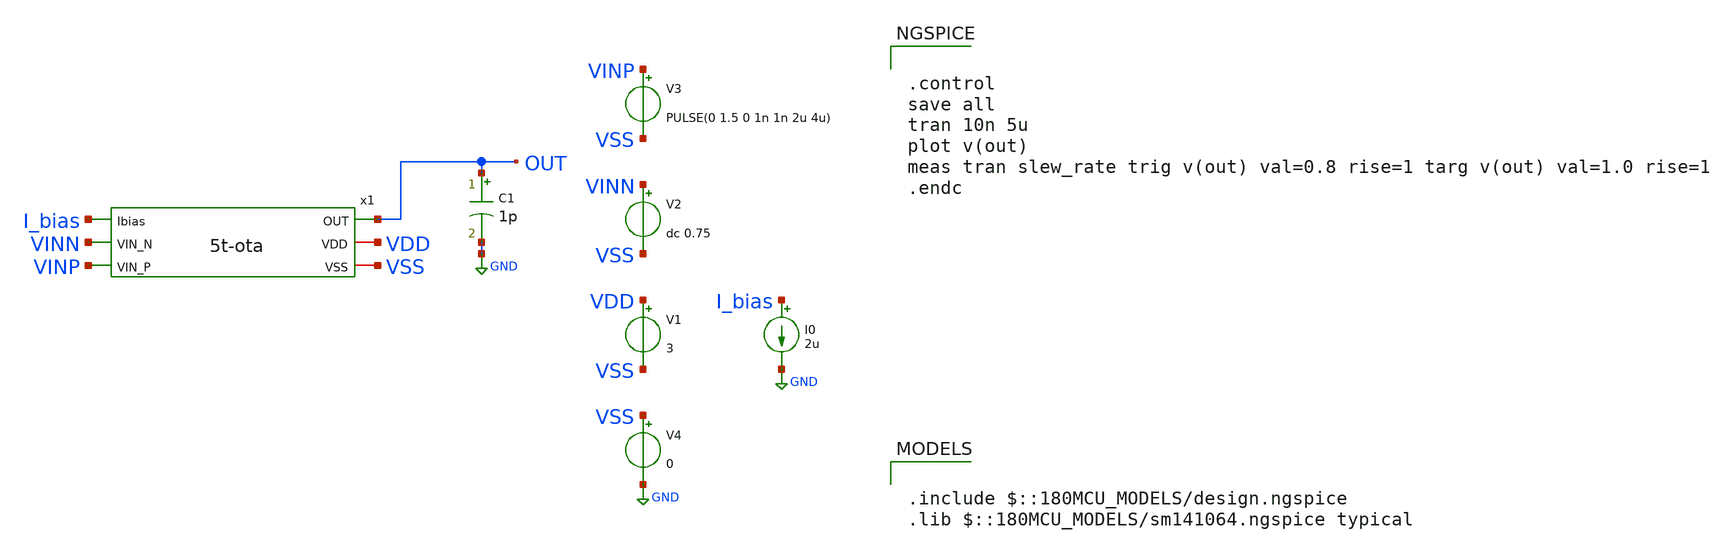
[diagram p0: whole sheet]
** sch_path: week02_current_diffpair/tugas5_cascode_current_mirror/5t-ota-psrr.sch
**.subckt 5t-ota-psrr
V1 VDD VSS 3
V2 VINN VSS dc 0.75
V3 VINP VSS PULSE(0 1.5 0 1n 1n 2u 4u)
V4 VSS GND 0
I0 I_bias GND 2u
x1 I_bias VINN VINP OUT VDD VSS 5t-ota
C1 OUT GND 1p m=1
**** begin user architecture code

.include $::180MCU_MODELS/design.ngspice
.lib $::180MCU_MODELS/sm141064.ngspice typical



.control
save all
tran 10n 5u
plot v(out)
meas tran slew_rate trig v(out) val=0.8 rise=1 targ v(out) val=1.0 rise=1
.endc


**** end user architecture code
**.ends

* expanding   symbol:  5t-ota.sym # of pins=6
** sym_path: week02_current_diffpair/tugas5_cascode_current_mirror/5t-ota.sym
** sch_path: week02_current_diffpair/tugas5_cascode_current_mirror/5t-ota.sch
.subckt 5t-ota Ibias VIN_N VIN_P OUT VDD VSS
*.ipin VIN_N
*.ipin VIN_P
*.opin OUT
*.iopin VDD
*.iopin VSS
*.ipin Ibias
XM4 net1 Ibias VSS VSS nfet_06v0 L=1u W=2.5u nf=1 ad='int((nf+1)/2) * W/nf * 0.18u' as='int((nf+2)/2) * W/nf * 0.18u'
+ pd='2*int((nf+1)/2) * (W/nf + 0.18u)' ps='2*int((nf+2)/2) * (W/nf + 0.18u)' nrd='0.18u / W' nrs='0.18u / W'
+ sa=0 sb=0 sd=0 m=1
XM8 Ibias Ibias VSS VSS nfet_06v0 L=1u W=5u nf=1 ad='int((nf+1)/2) * W/nf * 0.18u' as='int((nf+2)/2) * W/nf * 0.18u'
+ pd='2*int((nf+1)/2) * (W/nf + 0.18u)' ps='2*int((nf+2)/2) * (W/nf + 0.18u)' nrd='0.18u / W' nrs='0.18u / W'
+ sa=0 sb=0 sd=0 m=1
XM9 net2 net2 VDD VDD pfet_06v0 L=1u W=5u nf=1 ad='int((nf+1)/2) * W/nf * 0.18u' as='int((nf+2)/2) * W/nf * 0.18u'
+ pd='2*int((nf+1)/2) * (W/nf + 0.18u)' ps='2*int((nf+2)/2) * (W/nf + 0.18u)' nrd='0.18u / W' nrs='0.18u / W'
+ sa=0 sb=0 sd=0 m=1
XM10 OUT VIN_P net1 VSS nfet_06v0 L=1u W=20u nf=1 ad='int((nf+1)/2) * W/nf * 0.18u' as='int((nf+2)/2) * W/nf * 0.18u'
+ pd='2*int((nf+1)/2) * (W/nf + 0.18u)' ps='2*int((nf+2)/2) * (W/nf + 0.18u)' nrd='0.18u / W' nrs='0.18u / W'
+ sa=0 sb=0 sd=0 m=1
XM11 net2 VIN_N net1 VSS nfet_06v0 L=1u W=20u nf=1 ad='int((nf+1)/2) * W/nf * 0.18u' as='int((nf+2)/2) * W/nf * 0.18u'
+ pd='2*int((nf+1)/2) * (W/nf + 0.18u)' ps='2*int((nf+2)/2) * (W/nf + 0.18u)' nrd='0.18u / W' nrs='0.18u / W'
+ sa=0 sb=0 sd=0 m=1
XM12 OUT net2 VDD VDD pfet_06v0 L=1u W=5u nf=1 ad='int((nf+1)/2) * W/nf * 0.18u' as='int((nf+2)/2) * W/nf * 0.18u'
+ pd='2*int((nf+1)/2) * (W/nf + 0.18u)' ps='2*int((nf+2)/2) * (W/nf + 0.18u)' nrd='0.18u / W' nrs='0.18u / W'
+ sa=0 sb=0 sd=0 m=1
.ends

.GLOBAL GND
.end
